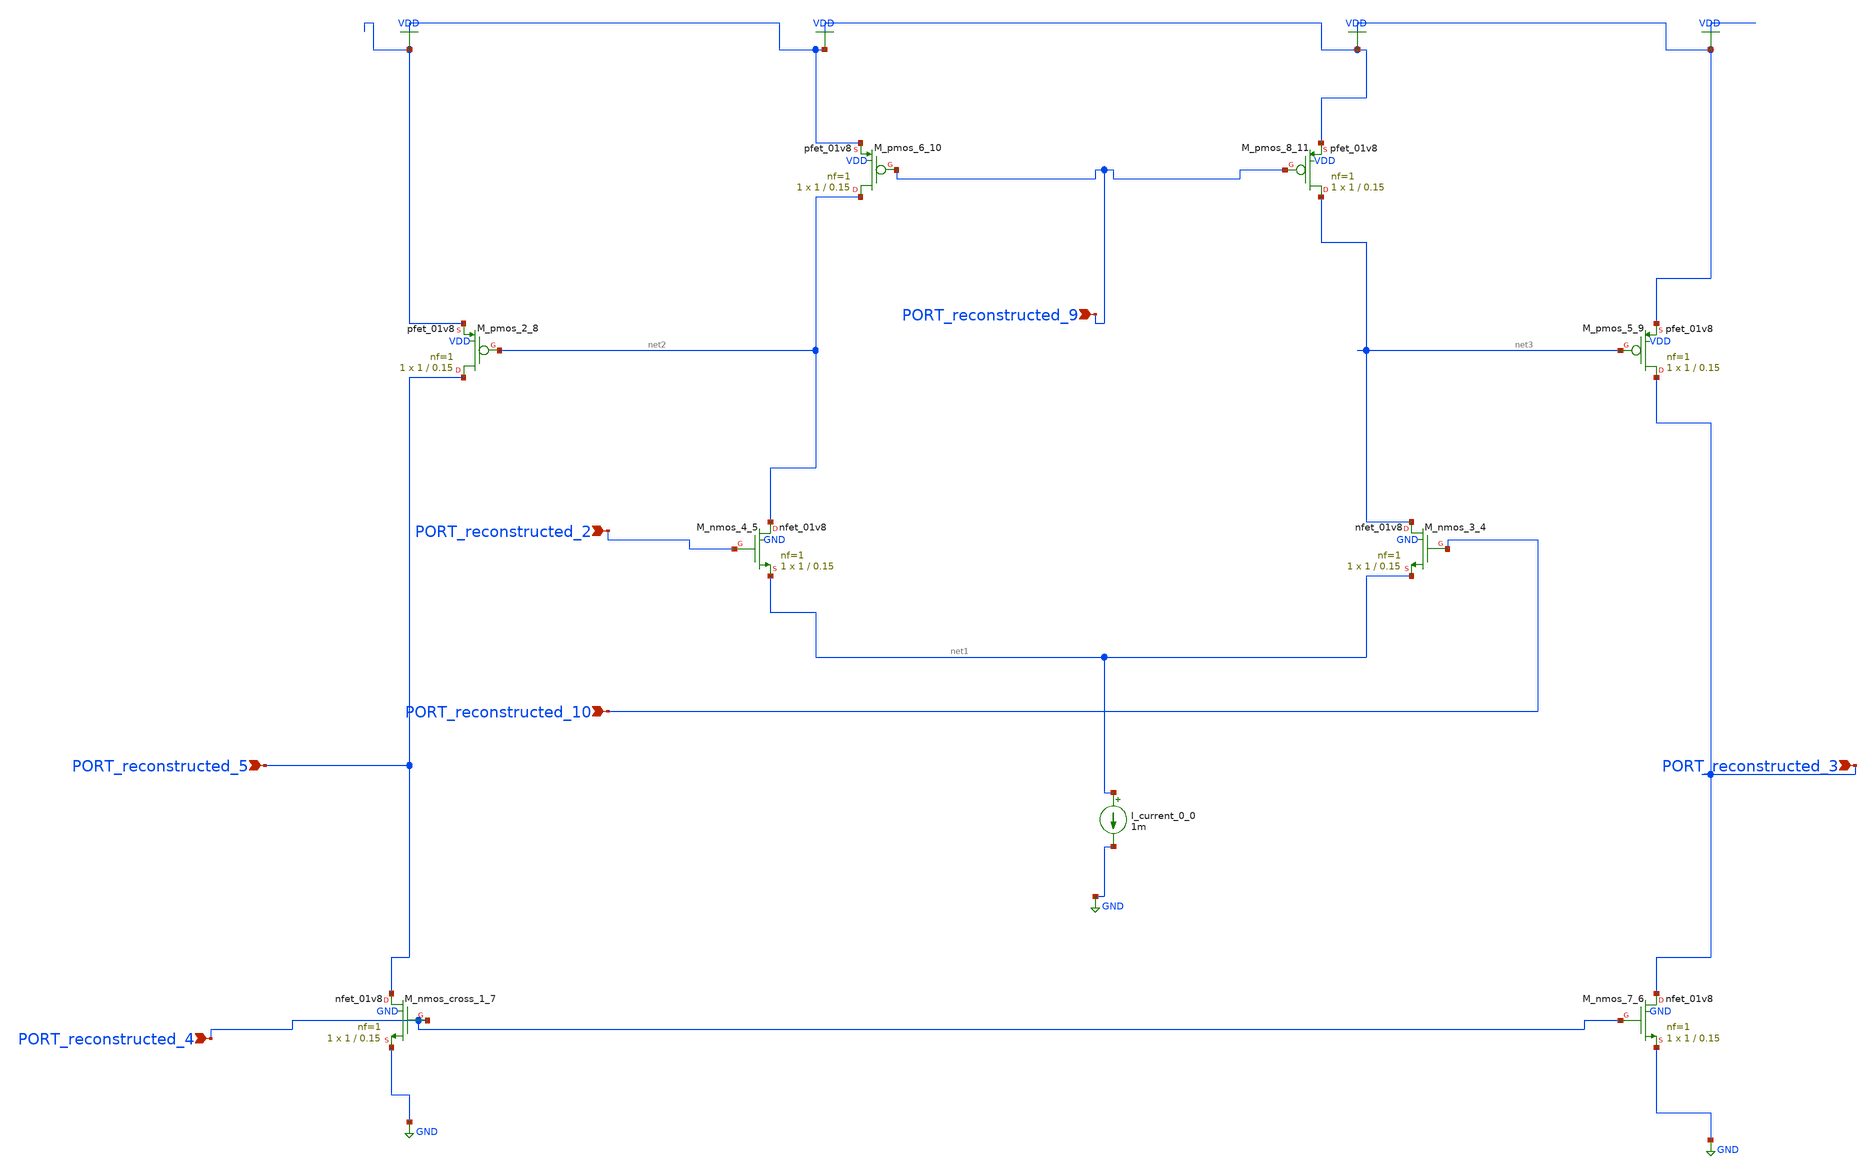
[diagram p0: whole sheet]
** sch_path: schematics/AMSNet/645.sch
**.subckt 645 PORT_reconstructed_3 PORT_reconstructed_10 PORT_reconstructed_5 PORT_reconstructed_2
*+ PORT_reconstructed_4 PORT_reconstructed_9
*.ipin PORT_reconstructed_3
*.ipin PORT_reconstructed_10
*.ipin PORT_reconstructed_5
*.ipin PORT_reconstructed_2
*.ipin PORT_reconstructed_4
*.ipin PORT_reconstructed_9
I_current_0_0 net1 GND 1m
XM_nmos_3_4 net3 PORT_reconstructed_10 net1 GND sky130_fd_pr__nfet_01v8 L=0.15 W=1 nf=1 ad='int((1 + 1)/2) * 1 / 1 * 0.29'
+ as='int((1 + 2)/2) * 1 / 1 * 0.29' pd='2*int((1 + 1)/2) * (1 / 1 + 0.29)' ps='2*int((1 + 2)/2) * (1 / 1 + 0.29)'
+ nrd='0.29 / 1 ' nrs='0.29 / 1 ' sa=0 sb=0 sd=0 mult=1 m=1
XM_nmos_4_5 net2 PORT_reconstructed_2 net1 GND sky130_fd_pr__nfet_01v8 L=0.15 W=1 nf=1 ad='int((1 + 1)/2) * 1 / 1 * 0.29'
+ as='int((1 + 2)/2) * 1 / 1 * 0.29' pd='2*int((1 + 1)/2) * (1 / 1 + 0.29)' ps='2*int((1 + 2)/2) * (1 / 1 + 0.29)'
+ nrd='0.29 / 1 ' nrs='0.29 / 1 ' sa=0 sb=0 sd=0 mult=1 m=1
XM_nmos_7_6 PORT_reconstructed_3 PORT_reconstructed_4 GND GND sky130_fd_pr__nfet_01v8 L=0.15 W=1 nf=1
+ ad='int((1 + 1)/2) * 1 / 1 * 0.29' as='int((1 + 2)/2) * 1 / 1 * 0.29' pd='2*int((1 + 1)/2) * (1 / 1 + 0.29)'
+ ps='2*int((1 + 2)/2) * (1 / 1 + 0.29)' nrd='0.29 / 1 ' nrs='0.29 / 1 ' sa=0 sb=0 sd=0 mult=1 m=1
XM_nmos_cross_1_7 PORT_reconstructed_5 PORT_reconstructed_4 GND GND sky130_fd_pr__nfet_01v8 L=0.15 W=1
+ nf=1 ad='int((1 + 1)/2) * 1 / 1 * 0.29' as='int((1 + 2)/2) * 1 / 1 * 0.29' pd='2*int((1 + 1)/2) * (1 / 1 + 0.29)'
+ ps='2*int((1 + 2)/2) * (1 / 1 + 0.29)' nrd='0.29 / 1 ' nrs='0.29 / 1 ' sa=0 sb=0 sd=0 mult=1 m=1
XM_pmos_2_8 PORT_reconstructed_5 net2 VDD VDD sky130_fd_pr__pfet_01v8 L=0.15 W=1 nf=1 ad='int((1 + 1)/2) * 1 / 1 * 0.29'
+ as='int((1 + 2)/2) * 1 / 1 * 0.29' pd='2*int((1 + 1)/2) * (1 / 1 + 0.29)' ps='2*int((1 + 2)/2) * (1 / 1 + 0.29)'
+ nrd='0.29 / 1 ' nrs='0.29 / 1 ' sa=0 sb=0 sd=0 mult=1 m=1
XM_pmos_5_9 PORT_reconstructed_3 net3 VDD VDD sky130_fd_pr__pfet_01v8 L=0.15 W=1 nf=1 ad='int((1 + 1)/2) * 1 / 1 * 0.29'
+ as='int((1 + 2)/2) * 1 / 1 * 0.29' pd='2*int((1 + 1)/2) * (1 / 1 + 0.29)' ps='2*int((1 + 2)/2) * (1 / 1 + 0.29)'
+ nrd='0.29 / 1 ' nrs='0.29 / 1 ' sa=0 sb=0 sd=0 mult=1 m=1
XM_pmos_6_10 net2 PORT_reconstructed_9 VDD VDD sky130_fd_pr__pfet_01v8 L=0.15 W=1 nf=1 ad='int((1 + 1)/2) * 1 / 1 * 0.29'
+ as='int((1 + 2)/2) * 1 / 1 * 0.29' pd='2*int((1 + 1)/2) * (1 / 1 + 0.29)' ps='2*int((1 + 2)/2) * (1 / 1 + 0.29)'
+ nrd='0.29 / 1 ' nrs='0.29 / 1 ' sa=0 sb=0 sd=0 mult=1 m=1
XM_pmos_8_11 net3 PORT_reconstructed_9 VDD VDD sky130_fd_pr__pfet_01v8 L=0.15 W=1 nf=1 ad='int((1 + 1)/2) * 1 / 1 * 0.29'
+ as='int((1 + 2)/2) * 1 / 1 * 0.29' pd='2*int((1 + 1)/2) * (1 / 1 + 0.29)' ps='2*int((1 + 2)/2) * (1 / 1 + 0.29)'
+ nrd='0.29 / 1 ' nrs='0.29 / 1 ' sa=0 sb=0 sd=0 mult=1 m=1
**.ends
.GLOBAL GND
.GLOBAL VDD
.end
